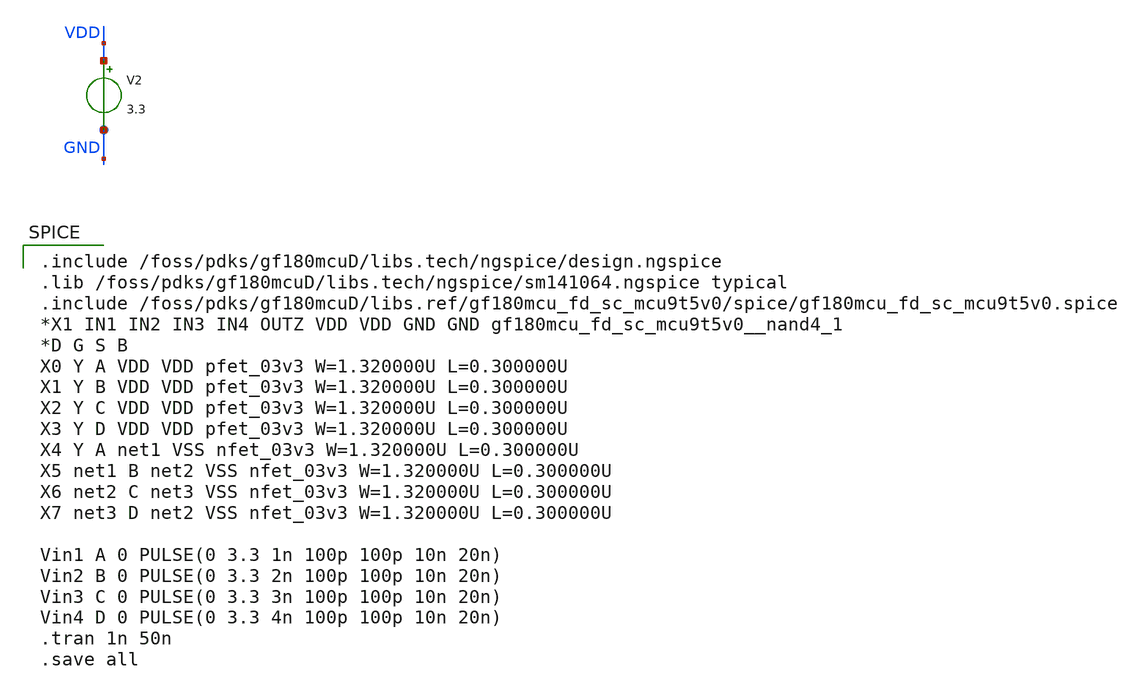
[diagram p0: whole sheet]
** sch_path: designs/libs/tb_NAND4/nand4_test.sch
**.subckt nand4_test
V2 VDD GND 3.3
**** begin user architecture code

.include /foss/pdks/gf180mcuD/libs.tech/ngspice/design.ngspice
.lib /foss/pdks/gf180mcuD/libs.tech/ngspice/sm141064.ngspice typical
.include /foss/pdks/gf180mcuD/libs.ref/gf180mcu_fd_sc_mcu9t5v0/spice/gf180mcu_fd_sc_mcu9t5v0.spice
*X1 IN1 IN2 IN3 IN4 OUTZ VDD VDD GND GND gf180mcu_fd_sc_mcu9t5v0__nand4_1
*D G S B
X0 Y A VDD VDD pfet_03v3 W=1.320000U L=0.300000U
X1 Y B VDD VDD pfet_03v3 W=1.320000U L=0.300000U
X2 Y C VDD VDD pfet_03v3 W=1.320000U L=0.300000U
X3 Y D VDD VDD pfet_03v3 W=1.320000U L=0.300000U
X4 Y A net1 VSS nfet_03v3 W=1.320000U L=0.300000U
X5 net1 B net2 VSS nfet_03v3 W=1.320000U L=0.300000U
X6 net2 C net3 VSS nfet_03v3 W=1.320000U L=0.300000U
X7 net3 D net2 VSS nfet_03v3 W=1.320000U L=0.300000U

Vin1 A 0 PULSE(0 3.3 1n 100p 100p 10n 20n)
Vin2 B 0 PULSE(0 3.3 2n 100p 100p 10n 20n)
Vin3 C 0 PULSE(0 3.3 3n 100p 100p 10n 20n)
Vin4 D 0 PULSE(0 3.3 4n 100p 100p 10n 20n)
.tran 1n 50n
.save all

**** end user architecture code
**.ends
.end
